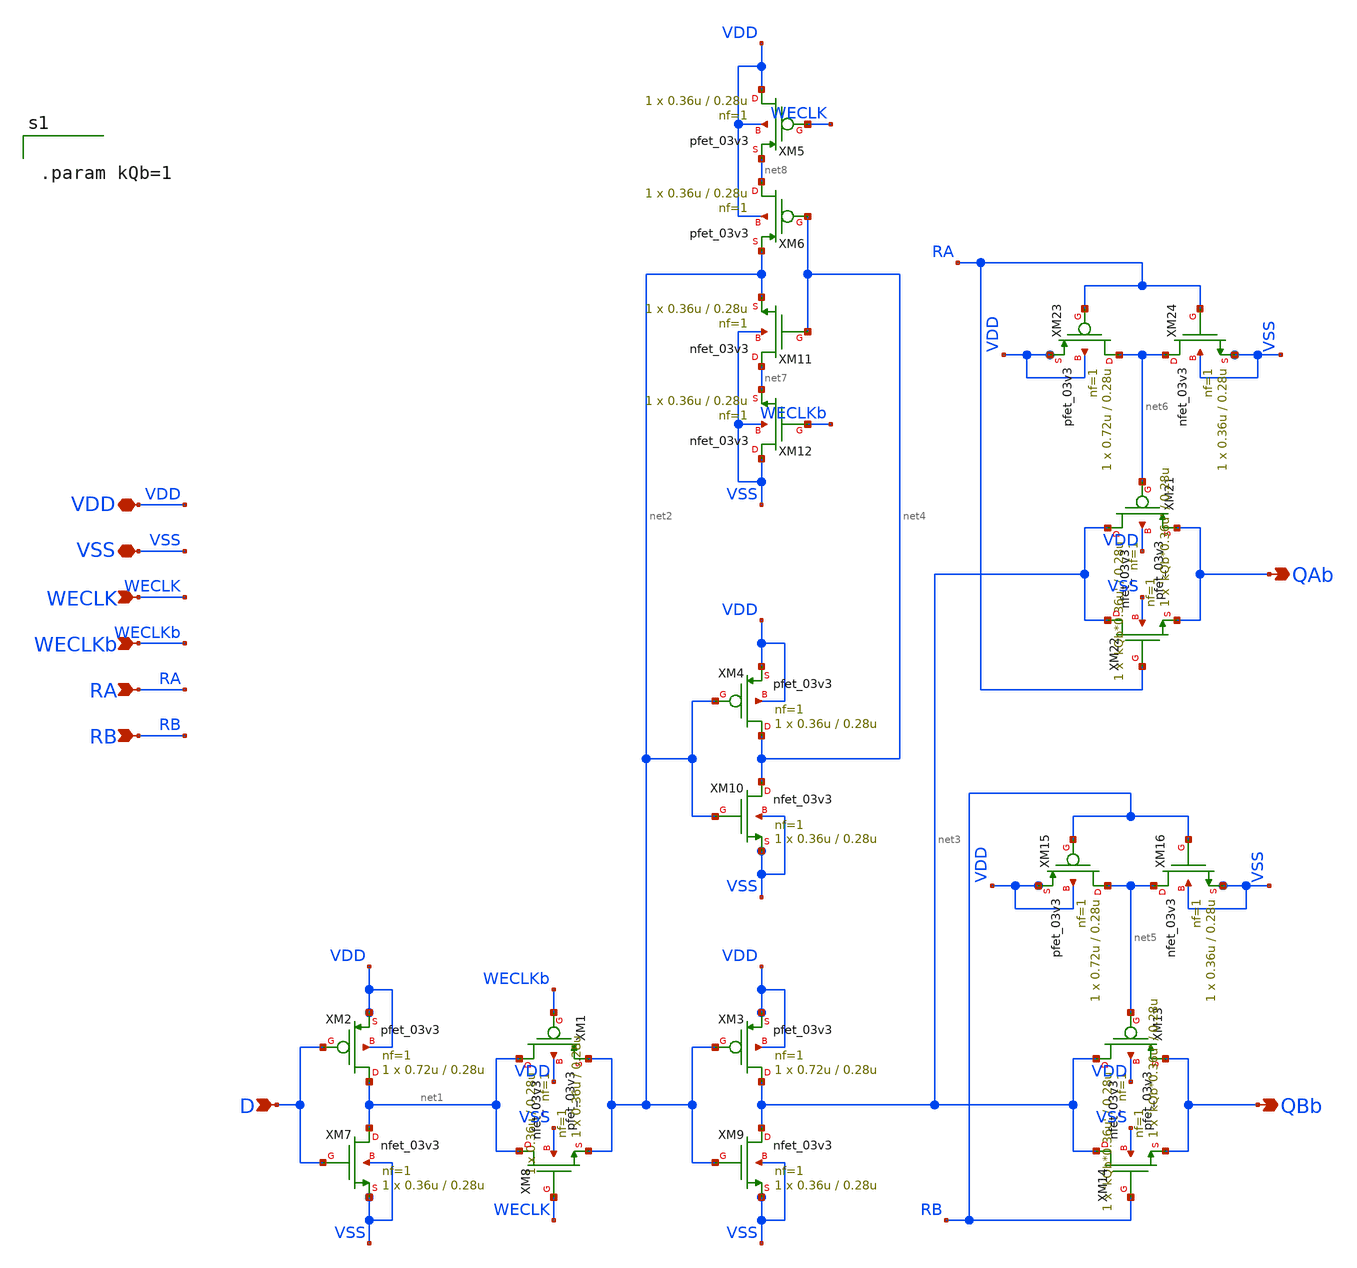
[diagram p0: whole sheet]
** sch_path: CAD3/slave_latch.sch
**.subckt slave_latch D RA RB WECLKb WECLK QAb QBb VDD VSS
*.ipin D
*.ipin RA
*.ipin RB
*.ipin WECLKb
*.ipin WECLK
*.opin QAb
*.opin QBb
*.iopin VDD
*.iopin VSS
XM1 net1 WECLKb net2 VDD pfet_03v3 L=0.28u W=0.36u nf=1 ad='int((nf+1)/2) * W/nf * 0.18u' as='int((nf+2)/2) * W/nf * 0.18u'
+ pd='2*int((nf+1)/2) * (W/nf + 0.18u)' ps='2*int((nf+2)/2) * (W/nf + 0.18u)' nrd='0.18u / W' nrs='0.18u / W'
+ sa=0 sb=0 sd=0 m=1
XM2 net1 D VDD VDD pfet_03v3 L=0.28u W=0.72u nf=1 ad='int((nf+1)/2) * W/nf * 0.18u' as='int((nf+2)/2) * W/nf * 0.18u'
+ pd='2*int((nf+1)/2) * (W/nf + 0.18u)' ps='2*int((nf+2)/2) * (W/nf + 0.18u)' nrd='0.18u / W' nrs='0.18u / W'
+ sa=0 sb=0 sd=0 m=1
XM3 net3 net2 VDD VDD pfet_03v3 L=0.28u W=0.72u nf=1 ad='int((nf+1)/2) * W/nf * 0.18u' as='int((nf+2)/2) * W/nf * 0.18u'
+ pd='2*int((nf+1)/2) * (W/nf + 0.18u)' ps='2*int((nf+2)/2) * (W/nf + 0.18u)' nrd='0.18u / W' nrs='0.18u / W'
+ sa=0 sb=0 sd=0 m=1
XM4 net4 net2 VDD VDD pfet_03v3 L=0.28u W=0.36u nf=1 ad='int((nf+1)/2) * W/nf * 0.18u' as='int((nf+2)/2) * W/nf * 0.18u'
+ pd='2*int((nf+1)/2) * (W/nf + 0.18u)' ps='2*int((nf+2)/2) * (W/nf + 0.18u)' nrd='0.18u / W' nrs='0.18u / W'
+ sa=0 sb=0 sd=0 m=1
XM5 VDD WECLK net8 VDD pfet_03v3 L=0.28u W=0.36u nf=1 ad='int((nf+1)/2) * W/nf * 0.18u' as='int((nf+2)/2) * W/nf * 0.18u'
+ pd='2*int((nf+1)/2) * (W/nf + 0.18u)' ps='2*int((nf+2)/2) * (W/nf + 0.18u)' nrd='0.18u / W' nrs='0.18u / W'
+ sa=0 sb=0 sd=0 m=1
XM6 net8 net4 net2 VDD pfet_03v3 L=0.28u W=0.36u nf=1 ad='int((nf+1)/2) * W/nf * 0.18u' as='int((nf+2)/2) * W/nf * 0.18u'
+ pd='2*int((nf+1)/2) * (W/nf + 0.18u)' ps='2*int((nf+2)/2) * (W/nf + 0.18u)' nrd='0.18u / W' nrs='0.18u / W'
+ sa=0 sb=0 sd=0 m=1
XM7 net1 D VSS VSS nfet_03v3 L=0.28u W=0.36u nf=1 ad='int((nf+1)/2) * W/nf * 0.18u' as='int((nf+2)/2) * W/nf * 0.18u'
+ pd='2*int((nf+1)/2) * (W/nf + 0.18u)' ps='2*int((nf+2)/2) * (W/nf + 0.18u)' nrd='0.18u / W' nrs='0.18u / W'
+ sa=0 sb=0 sd=0 m=1
XM8 net1 WECLK net2 VSS nfet_03v3 L=0.28u W=0.36u nf=1 ad='int((nf+1)/2) * W/nf * 0.18u' as='int((nf+2)/2) * W/nf * 0.18u'
+ pd='2*int((nf+1)/2) * (W/nf + 0.18u)' ps='2*int((nf+2)/2) * (W/nf + 0.18u)' nrd='0.18u / W' nrs='0.18u / W'
+ sa=0 sb=0 sd=0 m=1
XM9 net3 net2 VSS VSS nfet_03v3 L=0.28u W=0.36u nf=1 ad='int((nf+1)/2) * W/nf * 0.18u' as='int((nf+2)/2) * W/nf * 0.18u'
+ pd='2*int((nf+1)/2) * (W/nf + 0.18u)' ps='2*int((nf+2)/2) * (W/nf + 0.18u)' nrd='0.18u / W' nrs='0.18u / W'
+ sa=0 sb=0 sd=0 m=1
XM10 net4 net2 VSS VSS nfet_03v3 L=0.28u W=0.36u nf=1 ad='int((nf+1)/2) * W/nf * 0.18u' as='int((nf+2)/2) * W/nf * 0.18u'
+ pd='2*int((nf+1)/2) * (W/nf + 0.18u)' ps='2*int((nf+2)/2) * (W/nf + 0.18u)' nrd='0.18u / W' nrs='0.18u / W'
+ sa=0 sb=0 sd=0 m=1
XM11 net7 net4 net2 VSS nfet_03v3 L=0.28u W=0.36u nf=1 ad='int((nf+1)/2) * W/nf * 0.18u' as='int((nf+2)/2) * W/nf * 0.18u'
+ pd='2*int((nf+1)/2) * (W/nf + 0.18u)' ps='2*int((nf+2)/2) * (W/nf + 0.18u)' nrd='0.18u / W' nrs='0.18u / W'
+ sa=0 sb=0 sd=0 m=1
XM12 VSS WECLKb net7 VSS nfet_03v3 L=0.28u W=0.36u nf=1 ad='int((nf+1)/2) * W/nf * 0.18u' as='int((nf+2)/2) * W/nf * 0.18u'
+ pd='2*int((nf+1)/2) * (W/nf + 0.18u)' ps='2*int((nf+2)/2) * (W/nf + 0.18u)' nrd='0.18u / W' nrs='0.18u / W'
+ sa=0 sb=0 sd=0 m=1
XM13 net3 net5 QBb VDD pfet_03v3 L=0.28u W='kQb*0.36u' nf=1 ad='int((nf+1)/2) * W/nf * 0.18u' as='int((nf+2)/2) * W/nf * 0.18u'
+ pd='2*int((nf+1)/2) * (W/nf + 0.18u)' ps='2*int((nf+2)/2) * (W/nf + 0.18u)' nrd='0.18u / W' nrs='0.18u / W'
+ sa=0 sb=0 sd=0 m=1
XM14 net3 RB QBb VSS nfet_03v3 L=0.28u W='kQb*0.36u' nf=1 ad='int((nf+1)/2) * W/nf * 0.18u' as='int((nf+2)/2) * W/nf * 0.18u'
+ pd='2*int((nf+1)/2) * (W/nf + 0.18u)' ps='2*int((nf+2)/2) * (W/nf + 0.18u)' nrd='0.18u / W' nrs='0.18u / W'
+ sa=0 sb=0 sd=0 m=1
XM15 net5 RB VDD VDD pfet_03v3 L=0.28u W=0.72u nf=1 ad='int((nf+1)/2) * W/nf * 0.18u' as='int((nf+2)/2) * W/nf * 0.18u'
+ pd='2*int((nf+1)/2) * (W/nf + 0.18u)' ps='2*int((nf+2)/2) * (W/nf + 0.18u)' nrd='0.18u / W' nrs='0.18u / W'
+ sa=0 sb=0 sd=0 m=1
XM16 net5 RB VSS VSS nfet_03v3 L=0.28u W=0.36u nf=1 ad='int((nf+1)/2) * W/nf * 0.18u' as='int((nf+2)/2) * W/nf * 0.18u'
+ pd='2*int((nf+1)/2) * (W/nf + 0.18u)' ps='2*int((nf+2)/2) * (W/nf + 0.18u)' nrd='0.18u / W' nrs='0.18u / W'
+ sa=0 sb=0 sd=0 m=1
XM21 net3 net6 QAb VDD pfet_03v3 L=0.28u W='kQb*0.36u' nf=1 ad='int((nf+1)/2) * W/nf * 0.18u' as='int((nf+2)/2) * W/nf * 0.18u'
+ pd='2*int((nf+1)/2) * (W/nf + 0.18u)' ps='2*int((nf+2)/2) * (W/nf + 0.18u)' nrd='0.18u / W' nrs='0.18u / W'
+ sa=0 sb=0 sd=0 m=1
XM22 net3 RA QAb VSS nfet_03v3 L=0.28u W='kQb*0.36u' nf=1 ad='int((nf+1)/2) * W/nf * 0.18u' as='int((nf+2)/2) * W/nf * 0.18u'
+ pd='2*int((nf+1)/2) * (W/nf + 0.18u)' ps='2*int((nf+2)/2) * (W/nf + 0.18u)' nrd='0.18u / W' nrs='0.18u / W'
+ sa=0 sb=0 sd=0 m=1
XM23 net6 RA VDD VDD pfet_03v3 L=0.28u W=0.72u nf=1 ad='int((nf+1)/2) * W/nf * 0.18u' as='int((nf+2)/2) * W/nf * 0.18u'
+ pd='2*int((nf+1)/2) * (W/nf + 0.18u)' ps='2*int((nf+2)/2) * (W/nf + 0.18u)' nrd='0.18u / W' nrs='0.18u / W'
+ sa=0 sb=0 sd=0 m=1
XM24 net6 RA VSS VSS nfet_03v3 L=0.28u W=0.36u nf=1 ad='int((nf+1)/2) * W/nf * 0.18u' as='int((nf+2)/2) * W/nf * 0.18u'
+ pd='2*int((nf+1)/2) * (W/nf + 0.18u)' ps='2*int((nf+2)/2) * (W/nf + 0.18u)' nrd='0.18u / W' nrs='0.18u / W'
+ sa=0 sb=0 sd=0 m=1
**** begin user architecture code


.param kQb=1


**** end user architecture code
**.ends
.end
